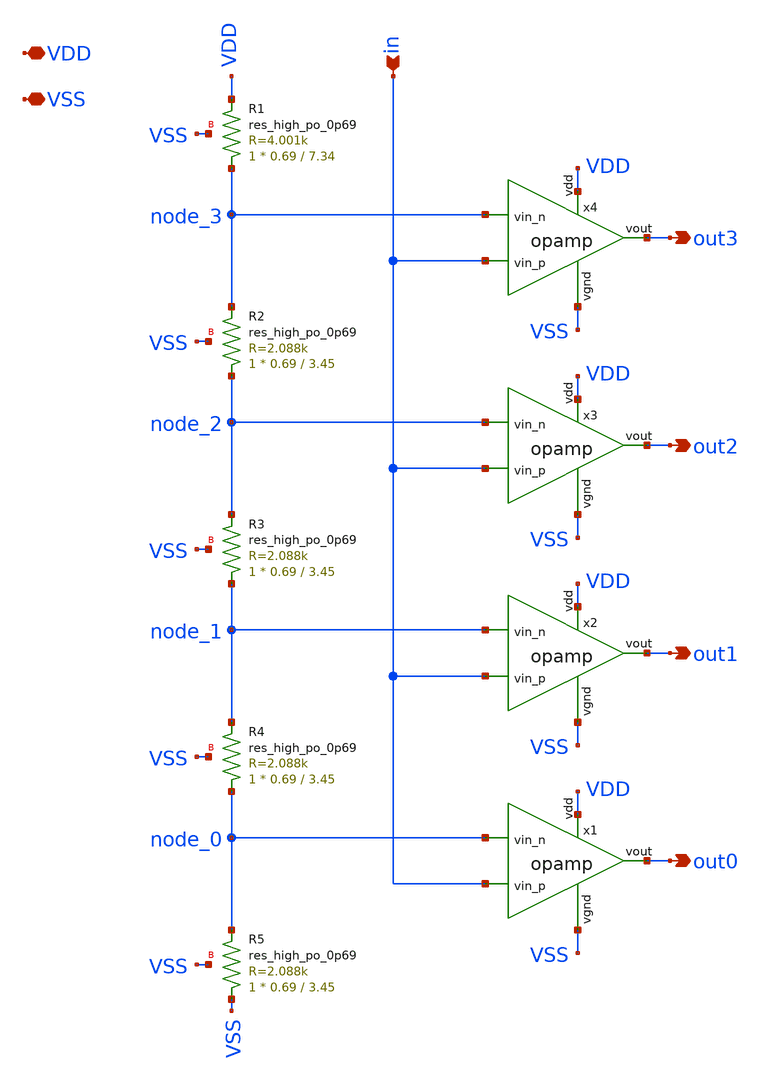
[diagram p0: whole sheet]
** sch_path: xschem/opamp_ladder.sch
**.subckt opamp_ladder out0 out2 out3 in VDD VSS out1
*.opin out0
*.opin out2
*.opin out3
*.ipin in
*.iopin VDD
*.iopin VSS
*.opin out1
x1 VDD node_0 in out0 VSS opamp
x2 VDD node_1 in out1 VSS opamp
x3 VDD node_2 in out2 VSS opamp
x4 VDD node_3 in out3 VSS opamp
XR1 node_3 VDD VSS sky130_fd_pr__res_high_po_0p69 L=7.34 mult=1 m=1
XR2 node_2 node_3 VSS sky130_fd_pr__res_high_po_0p69 L=3.45 mult=1 m=1
XR3 node_1 node_2 VSS sky130_fd_pr__res_high_po_0p69 L=3.45 mult=1 m=1
XR4 node_0 node_1 VSS sky130_fd_pr__res_high_po_0p69 L=3.45 mult=1 m=1
XR5 VSS node_0 VSS sky130_fd_pr__res_high_po_0p69 L=3.45 mult=1 m=1
**.ends

* expanding   symbol:  opamp.sym # of pins=5
** sym_path: xschem/opamp.sym
** sch_path: xschem/opamp.sch
.subckt opamp VDD vin_n vin_p Vout VGND
*.ipin vin_n
*.ipin vin_p
*.opin Vout
*.iopin VDD
*.iopin VGND
XM1 net1 vin_n net3 VDD sky130_fd_pr__pfet_01v8 L=0.6 W=6 nf=1 ad='W * 0.29' as='W * 0.29' pd='2 * (W + 0.29)'
+ ps='2 * (W + 0.29)' nrd='0.29 / W' nrs='0.29 / W' sa=0 sb=0 sd=0 mult=1 m=1
XM2 net2 vin_p net3 VDD sky130_fd_pr__pfet_01v8 L=0.6 W=6 nf=1 ad='W * 0.29' as='W * 0.29' pd='2 * (W + 0.29)'
+ ps='2 * (W + 0.29)' nrd='0.29 / W' nrs='0.29 / W' sa=0 sb=0 sd=0 mult=1 m=1
XM3 net1 net1 VGND VGND sky130_fd_pr__nfet_01v8 L=0.6 W=6 nf=1 ad='W * 0.29' as='W * 0.29' pd='2 * (W + 0.29)'
+ ps='2 * (W + 0.29)' nrd='0.29 / W' nrs='0.29 / W' sa=0 sb=0 sd=0 mult=1 m=1
XM4 net2 net1 VGND VGND sky130_fd_pr__nfet_01v8 L=0.6 W=6 nf=1 ad='W * 0.29' as='W * 0.29' pd='2 * (W + 0.29)'
+ ps='2 * (W + 0.29)' nrd='0.29 / W' nrs='0.29 / W' sa=0 sb=0 sd=0 mult=1 m=1
XM5 net3 net4 VDD VDD sky130_fd_pr__pfet_01v8 L=0.6 W=6 nf=1 ad='W * 0.29' as='W * 0.29' pd='2 * (W + 0.29)'
+ ps='2 * (W + 0.29)' nrd='0.29 / W' nrs='0.29 / W' sa=0 sb=0 sd=0 mult=1 m=1
XM7 Vout net2 VDD VDD sky130_fd_pr__pfet_01v8 L=0.15 W=3 nf=1 ad='W * 0.29' as='W * 0.29' pd='2 * (W + 0.29)'
+ ps='2 * (W + 0.29)' nrd='0.29 / W' nrs='0.29 / W' sa=0 sb=0 sd=0 mult=1 m=1
XM8 net4 net4 VDD VDD sky130_fd_pr__pfet_01v8 L=0.6 W=6 nf=1 ad='W * 0.29' as='W * 0.29' pd='2 * (W + 0.29)'
+ ps='2 * (W + 0.29)' nrd='0.29 / W' nrs='0.29 / W' sa=0 sb=0 sd=0 mult=1 m=1
XM6 Vout net2 VGND VGND sky130_fd_pr__nfet_01v8 L=0.15 W=1.5 nf=1 ad='W * 0.29' as='W * 0.29' pd='2 * (W + 0.29)'
+ ps='2 * (W + 0.29)' nrd='0.29 / W' nrs='0.29 / W' sa=0 sb=0 sd=0 mult=1 m=1
XR VGND net8 VGND sky130_fd_pr__res_high_po_0p35 L=4 mult=1 m=1
XR1 net8 net7 VGND sky130_fd_pr__res_high_po_0p35 L=4 mult=1 m=1
XR2 net7 net6 VGND sky130_fd_pr__res_high_po_0p35 L=4 mult=1 m=1
XR3 net6 net5 VGND sky130_fd_pr__res_high_po_0p35 L=4 mult=1 m=1
XR4 net5 net4 VGND sky130_fd_pr__res_high_po_0p35 L=4 mult=1 m=1
.ends

.end
